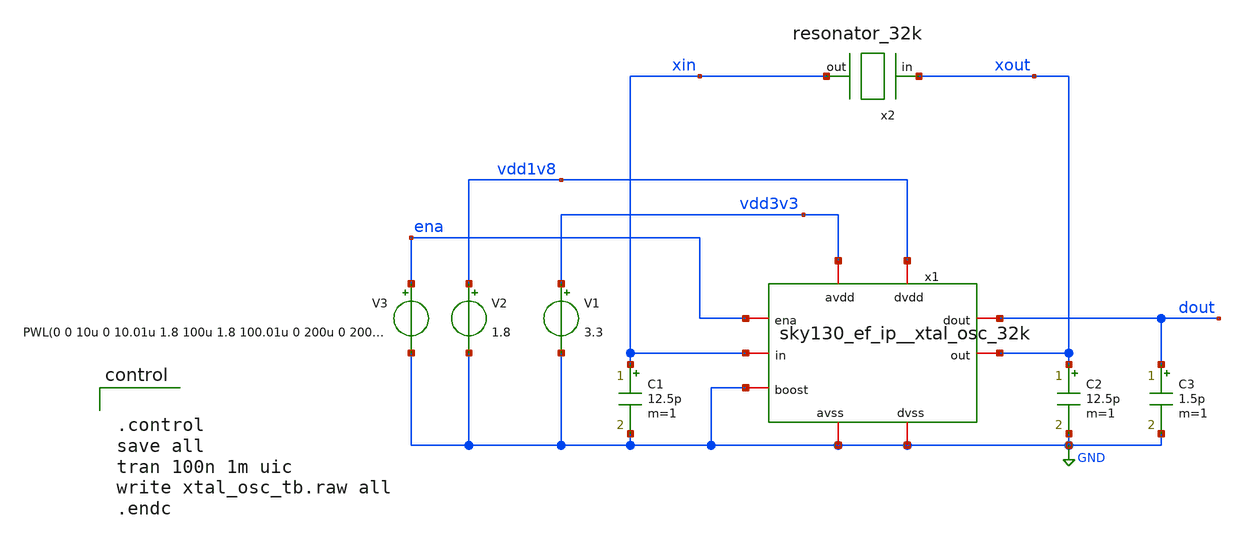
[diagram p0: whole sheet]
** sch_path: xschem/xtal_osc_tb.sch
**.subckt xtal_osc_tb
x1 ena vdd1v8 vdd3v3 xin xout GND GND dout GND sky130_ef_ip__xtal_osc_32k
x2 xout xin resonator_32k
V1 vdd3v3 GND 3.3
V2 vdd1v8 GND 1.8
C1 xin GND 12.5p m=1
C2 xout GND 12.5p m=1
C3 dout GND 1.5p m=1
V3 ena GND PWL(0 0 10u 0 10.01u 1.8 100u 1.8 100.01u 0 200u 0 200.01u 1.8)
**** begin user architecture code


.lib /usr/share/pdk/sky130A/libs.tech/ngspice/sky130.lib.spice tt




.control
save all
tran 100n 1m uic
write xtal_osc_tb.raw all
.endc


**** end user architecture code
**.ends
.GLOBAL GND
.end
